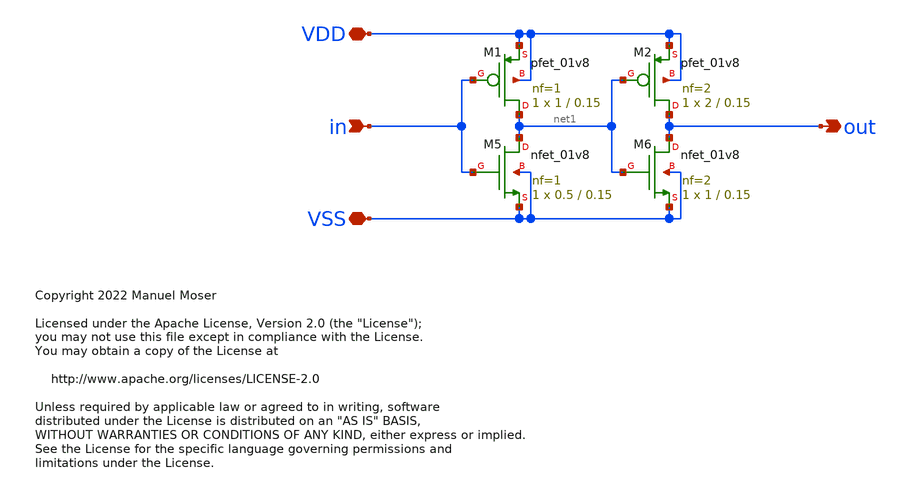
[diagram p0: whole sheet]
** sch_path: xschem/adc_comp_buffer/adc_comp_buffer.sch
* Copyright 2022 Manuel Moser
* Licensed under the Apache License, Version 2.0 (the "License");
**.subckt adc_comp_buffer in VDD VSS out
*.ipin in
*.iopin VDD
*.iopin VSS
*.opin out
XM1 net1 in VDD VDD sky130_fd_pr__pfet_01v8 L=0.15 W=1 nf=1 ad='int((nf+1)/2) * W/nf * 0.29' as='int((nf+2)/2) * W/nf * 0.29'
+ pd='2*int((nf+1)/2) * (W/nf + 0.29)' ps='2*int((nf+2)/2) * (W/nf + 0.29)' nrd='0.29 / W' nrs='0.29 / W'
+ sa=0 sb=0 sd=0 mult=1 m=1
XM2 out net1 VDD VDD sky130_fd_pr__pfet_01v8 L=0.15 W=2 nf=2 ad='int((nf+1)/2) * W/nf * 0.29' as='int((nf+2)/2) * W/nf * 0.29'
+ pd='2*int((nf+1)/2) * (W/nf + 0.29)' ps='2*int((nf+2)/2) * (W/nf + 0.29)' nrd='0.29 / W' nrs='0.29 / W'
+ sa=0 sb=0 sd=0 mult=1 m=1
XM5 net1 in VSS VSS sky130_fd_pr__nfet_01v8 L=0.15 W=0.5 nf=1 ad='int((nf+1)/2) * W/nf * 0.29' as='int((nf+2)/2) * W/nf * 0.29'
+ pd='2*int((nf+1)/2) * (W/nf + 0.29)' ps='2*int((nf+2)/2) * (W/nf + 0.29)' nrd='0.29 / W' nrs='0.29 / W'
+ sa=0 sb=0 sd=0 mult=1 m=1
XM6 out net1 VSS VSS sky130_fd_pr__nfet_01v8 L=0.15 W=1 nf=2 ad='int((nf+1)/2) * W/nf * 0.29' as='int((nf+2)/2) * W/nf * 0.29'
+ pd='2*int((nf+1)/2) * (W/nf + 0.29)' ps='2*int((nf+2)/2) * (W/nf + 0.29)' nrd='0.29 / W' nrs='0.29 / W'
+ sa=0 sb=0 sd=0 mult=1 m=1
**.ends
.end
